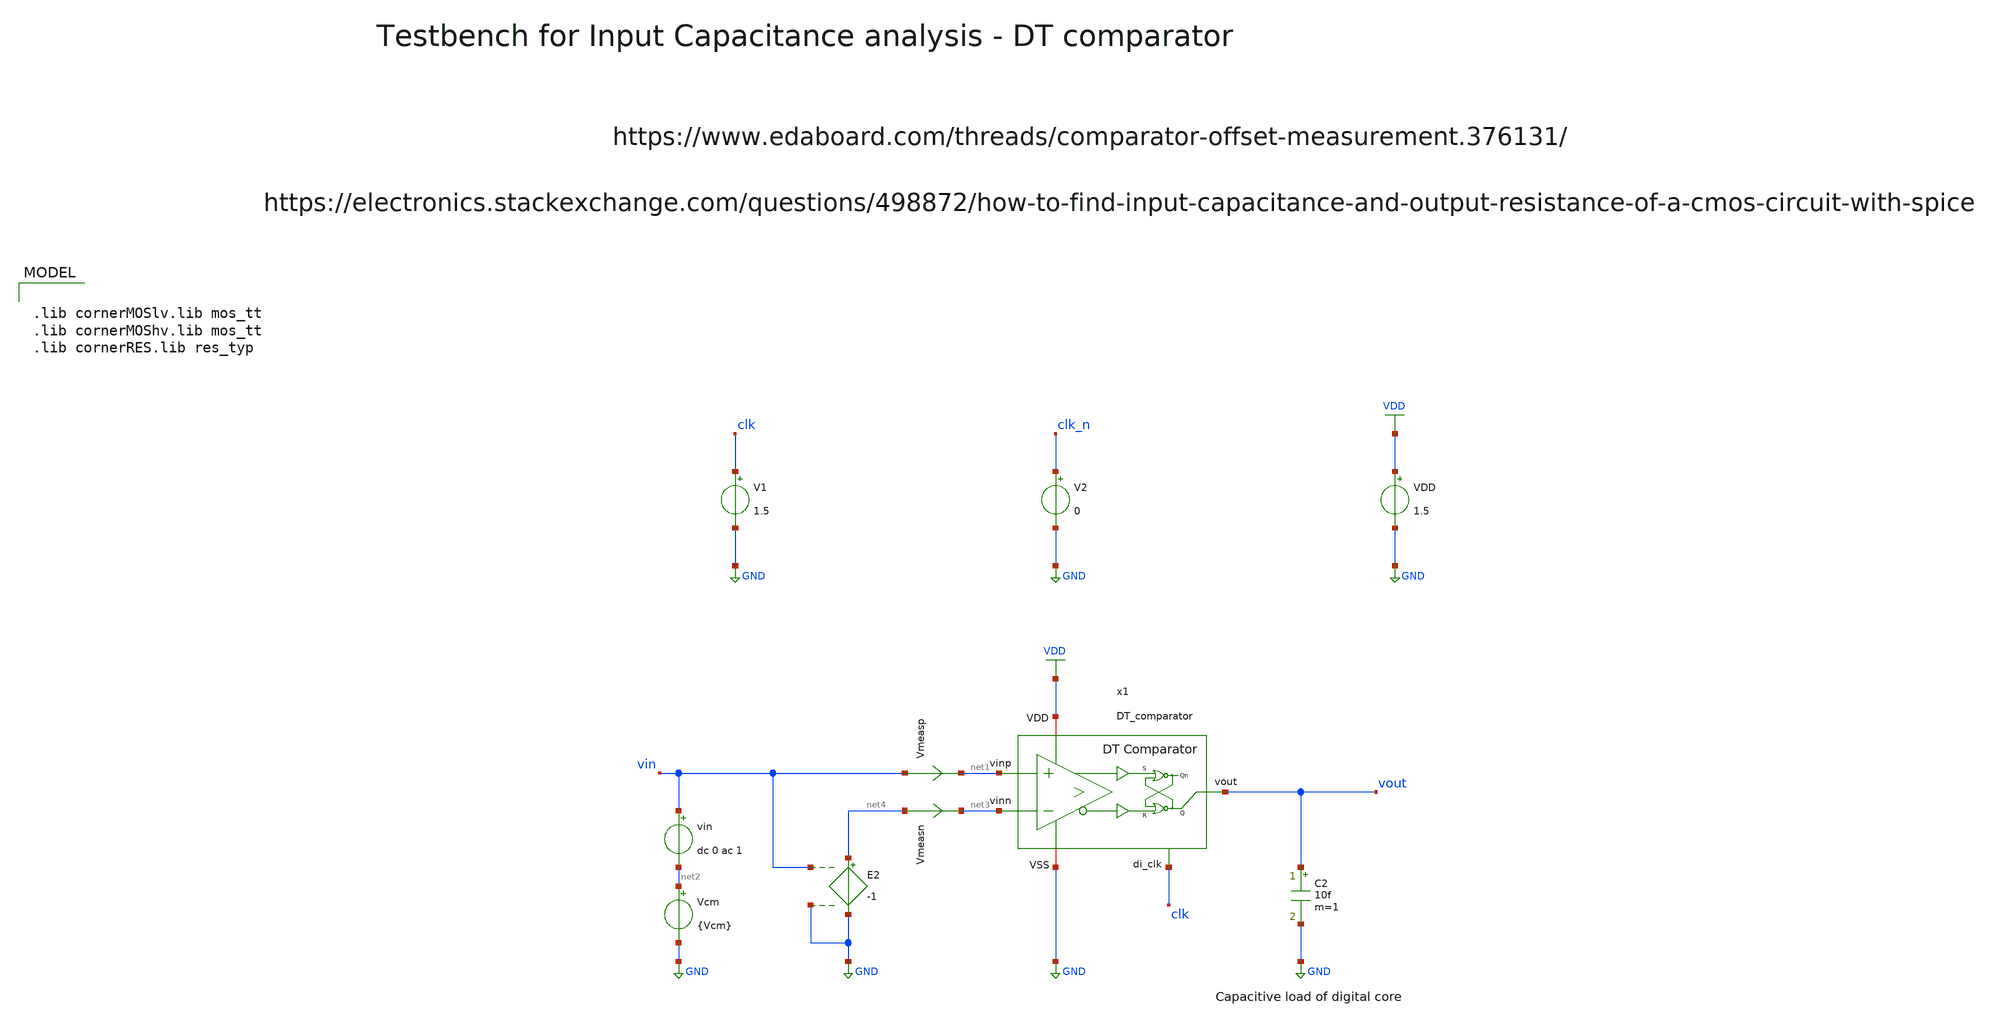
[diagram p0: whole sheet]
** sch_path: SG13G2_ATBS-ADC-main/xschem/comparator/discrete_time/testbenches/DT_comparator_tb_ac_cin.sch
**.subckt DT_comparator_tb_ac_cin
VDD VDD GND 1.5
V1 clk GND 1.5
V2 clk_n GND 0
Vmeasp vin net1 0
.save i(vmeasp)
Vmeasn net4 net3 0
.save i(vmeasn)
vin vin net2 dc 0 ac 1
Vcm net2 GND {Vcm}
E2 net4 GND vin GND -1
C2 vout GND 10f m=1
x1 VDD net1 vout net3 clk GND DT_comparator
**** begin user architecture code

.lib cornerMOSlv.lib mos_tt
.lib cornerMOShv.lib mos_tt
.lib cornerRES.lib res_typ



.param temp=27
.param Vcm=0.75
.options savecurrents reltol=1e-3 abstol=1e-12 gmin=1e-15
.control
save all

* User Constants
let fstart = 1
let fstop = 1G

* Operating Point Analysis
op
remzerovec
write DT_comparator_tb_ac_cin.raw
* set appendwrite

* AC Analysis
ac dec 101 $&fstart $&fstop
remzerovec
write DT_comparator_tb_ac_cin.raw

* Plotting Cinp
let Cinp = mag(i(Vmeasp)) / (2 * 3.14 * frequency)
plot Cinp

* Plotting Cinn
let Cinn = mag(i(Vmeasn)) / (2 * 3.14 * frequency)
plot Cinn

* Measure avg. Cinp & Cinn
meas ac Cinp_avg AVG Cinp from=fstart to=fstop
meas ac Cinn_avg AVG Cinn from=fstart to=fstop

* Writing Data
set wr_singlescale
set wr_vecnames
wrdata /foss/designs/SG13G2_ATBS-ADC-main/python/plot_simulations/data/DT_comparator_tb_ac_cin.txt
+ v(Cinp) v(Cinn)

*quit
.endc

**** end user architecture code
**.ends

* expanding   symbol:  comparator/discrete_time/DT_comparator.sym # of pins=6
** sym_path: SG13G2_ATBS-ADC-main/xschem/comparator/discrete_time/DT_comparator.sym
** sch_path: SG13G2_ATBS-ADC-main/xschem/comparator/discrete_time/DT_comparator.sch
.subckt DT_comparator VDD vinp vout vinn di_clk VSS
*.iopin VDD
*.opin vout
*.iopin VSS
*.ipin vinp
*.ipin vinn
*.ipin di_clk
x2 VDD voutp_comp voutp_buf VSS buffer_lv W_P_INV=1.0u L_P_INV=0.13u W_N_INV=1.0u L_N_INV=0.13u
x3 VDD voutn_comp voutn_buf VSS buffer_lv W_P_INV=1.0u L_P_INV=0.13u W_N_INV=1.0u L_N_INV=0.13u
x5 VDD di_clk net1 VSS inverter_lv W_P=1.0u L_P=0.13u W_N=1.0u L_N=0.13u
* noconn #net2
x4 VDD voutp_buf net2 VSS vout voutn_buf SR_latch W_P_SR=1.0u L_P_SR=0.13u W_N_SR=1.0u L_N_SR=0.13u
x1 net1 di_clk VDD voutp_comp vinp VSS voutn_comp vinn dynamic_biasing_comparator
.ends


* expanding   symbol:  buffer/buffer_lv.sym # of pins=4
** sym_path: SG13G2_ATBS-ADC-main/xschem/buffer/buffer_lv.sym
** sch_path: SG13G2_ATBS-ADC-main/xschem/buffer/buffer_lv.sch
.subckt buffer_lv VDD vin vout VSS  W_P_INV=3.0u L_P_INV=0.13u W_N_INV=1.0u L_N_INV=0.13u
*.ipin vin
*.iopin VDD
*.iopin VSS
*.opin vout
x1 VDD vin net1 VSS inverter_lv W_P=W_P_INV L_P=L_P_INV W_N=W_N_INV L_N=L_N_INV
x2 VDD net1 vout VSS inverter_lv W_P=W_P_INV L_P=L_P_INV W_N=W_N_INV L_N=L_N_INV
.ends


* expanding   symbol:  inverter/inverter_lv.sym # of pins=4
** sym_path: SG13G2_ATBS-ADC-main/xschem/inverter/inverter_lv.sym
** sch_path: SG13G2_ATBS-ADC-main/xschem/inverter/inverter_lv.sch
.subckt inverter_lv VDD vin vout VSS  W_P=3.0u L_P=0.13u W_N=1.0u L_N=0.13u
*.ipin vin
*.iopin VDD
*.iopin VSS
*.opin vout
XM1 vout vin VDD VDD sg13_lv_pmos w=W_P l=L_P ng=1 m=1 mm_ok=1
XM2 vout vin VSS VSS sg13_lv_nmos w=W_N l=L_N ng=1 m=1 mm_ok=1
.ends


* expanding   symbol:  comparator/SR_latch/SR_latch.sym # of pins=6
** sym_path: SG13G2_ATBS-ADC-main/xschem/comparator/SR_latch/SR_latch.sym
** sch_path: SG13G2_ATBS-ADC-main/xschem/comparator/SR_latch/SR_latch.sch
.subckt SR_latch VDD S Qn VSS Q R  W_P_SR=1.0u L_P_SR=0.13u W_N_SR=1.0u L_N_SR=0.13u
*.iopin VDD
*.opin Q
*.iopin VSS
*.ipin S
*.ipin R
*.opin Qn
x1 VDD Q R Qn VSS NOR_gate W_P=W_P_SR L_P=L_P_SR W_N=W_N_SR L_N=L_N_SR
x2 VDD Qn Q S VSS NOR_gate W_P=W_P_SR L_P=L_P_SR W_N=W_N_SR L_N=L_N_SR
.ends


* expanding   symbol:  comparator/discrete_time/Dynamic-biasing/dynamic_biasing_comparator.sym # of
*+ pins=8
** sym_path: SG13G2_ATBS-ADC-main/xschem/comparator/discrete_time/Dynamic-biasing/dynamic_biasing_comparator.sym
** sch_path: SG13G2_ATBS-ADC-main/xschem/comparator/discrete_time/Dynamic-biasing/dynamic_biasing_comparator.sch
.subckt dynamic_biasing_comparator di_clk_n di_clk VDD voutp vinp VSS voutn vinn
*.iopin VDD
*.opin voutp
*.opin voutn
*.ipin di_clk_n
*.iopin VSS
*.ipin vinp
*.ipin vinn
*.ipin di_clk
XM3a vs di_clk vctail VSS sg13_lv_nmos w=1.0u l=0.13u ng=1 m=1 mm_ok=1
XM12 voutp di_clk_n VSS VSS sg13_lv_nmos w=1.0u l=0.13u ng=1 m=1 mm_ok=1
XM8 net1 voutn VDD VDD sg13_lv_pmos w=2.0u l=0.13u ng=2 m=1 mm_ok=1
XM10 voutp voutn VSS VSS sg13_lv_nmos w=1.0u l=0.13u ng=1 m=1 mm_ok=1
XM11 voutn voutp VSS VSS sg13_lv_nmos w=1.0u l=0.13u ng=1 m=1 mm_ok=1
XM13 voutn di_clk_n VSS VSS sg13_lv_nmos w=1.0u l=0.13u ng=1 m=1 mm_ok=1
CPn vcpn VSS 300f m=1
CPp vcpp VSS 300f m=1
XM9 net2 voutp VDD VDD sg13_lv_pmos w=2.0u l=0.13u ng=2 m=1 mm_ok=1
XM6 voutp vcpn net1 VDD sg13_lv_pmos w=2.0u l=0.13u ng=2 m=1 mm_ok=1
XM7 voutn vcpp net2 VDD sg13_lv_pmos w=2.0u l=0.13u ng=2 m=1 mm_ok=1
CTAIL vctail VSS 600f m=1
XM3b vctail di_clk_n VSS VSS sg13_lv_nmos w=1.0u l=0.13u ng=1 m=1 mm_ok=1
XM1 vcpn vinp vs VSS sg13_lv_nmos w=1.0u l=0.13u ng=1 m=1 mm_ok=1
XM2 vcpp vinn vs VSS sg13_lv_nmos w=1.0u l=0.13u ng=1 m=1 mm_ok=1
XM4 vcpn di_clk VDD VDD sg13_lv_pmos w=1.0u l=0.13u ng=1 m=1 mm_ok=1
XM5 vcpp di_clk VDD VDD sg13_lv_pmos w=1.0u l=0.13u ng=1 m=1 mm_ok=1
.ends


* expanding   symbol:  comparator/NOR_gate/NOR_gate.sym # of pins=5
** sym_path: SG13G2_ATBS-ADC-main/xschem/comparator/NOR_gate/NOR_gate.sym
** sch_path: SG13G2_ATBS-ADC-main/xschem/comparator/NOR_gate/NOR_gate.sch
.subckt NOR_gate VDD C A B VSS  W_P=1.0u L_P=0.13u W_N=0.5u L_N=0.13u
*.iopin VDD
*.opin C
*.iopin VSS
*.ipin A
*.ipin B
XM1 C A VSS VSS sg13_lv_nmos w=W_N l=L_N ng=1 m=1 mm_ok=1
XM2 C B VSS VSS sg13_lv_nmos w=W_N l=L_N ng=1 m=1 mm_ok=1
XM3 C B net1 VDD sg13_lv_pmos w=W_P l=L_P ng=1 m=1 mm_ok=1
XM4 net1 A VDD VDD sg13_lv_pmos w=W_P l=L_P ng=1 m=1 mm_ok=1
XM5 C A net2 VDD sg13_lv_pmos w=W_P l=L_P ng=1 m=1 mm_ok=1
XM6 net2 B VDD VDD sg13_lv_pmos w=W_P l=L_P ng=1 m=1 mm_ok=1
.ends

.GLOBAL GND
.GLOBAL VDD
.end
